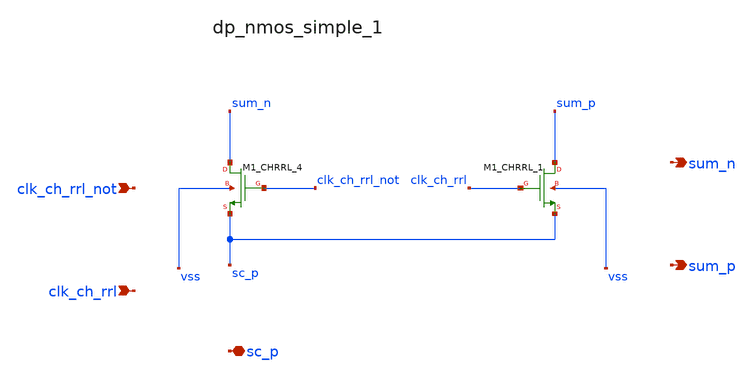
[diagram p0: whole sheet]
** sch_path: analog-db/raw/sup_003_rrl_sc_integrator/hier/blocks/dp_nmos_simple_1.sch
**.subckt dp_nmos_simple_1 clk_ch_rrl_not clk_ch_rrl sc_p sum_n sum_p
*.ipin clk_ch_rrl_not
*.ipin clk_ch_rrl
*.iopin sc_p
*.opin sum_n
*.opin sum_p
XM1_CHRRL_1 sum_p clk_ch_rrl sc_p vss sg13_lv_nmos w=x_dut_xm1_chrrl_1_w l=x_dut_xm1_chrrl_1_l ng=1
+ m=x_dut_xm1_chrrl_1_m
XM1_CHRRL_4 sum_n clk_ch_rrl_not sc_p vss sg13_lv_nmos w=x_dut_xm1_chrrl_4_w l=x_dut_xm1_chrrl_4_l
+ ng=1 m=x_dut_xm1_chrrl_4_m
**.ends
.end
